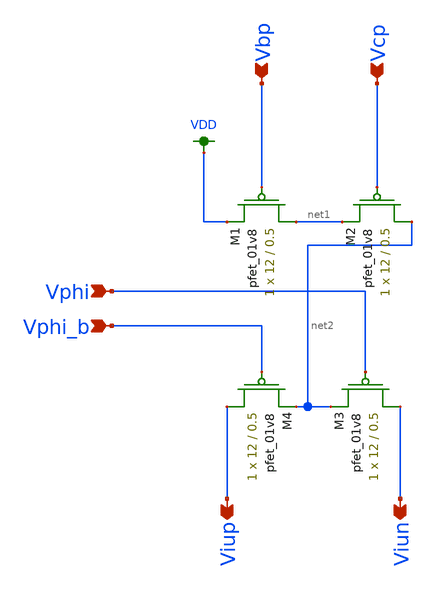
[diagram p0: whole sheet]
** sch_path: simulation/dac/dac_unit_lds.sch
**.subckt dac_unit_lds Vphi Vbp Vcp Viun Viup Vphi_b
*.ipin Vphi
*.ipin Vbp
*.ipin Vcp
*.opin Viun
*.opin Viup
*.ipin Vphi_b
XM1 net1 Vbp VDD VDD sky130_fd_pr__pfet_01v8 L=0.5 W=12 nf=1 ad='int((nf+1)/2) * W/nf * 0.29' as='int((nf+2)/2) * W/nf * 0.29'
+ pd='2*int((nf+1)/2) * (W/nf + 0.29)' ps='2*int((nf+2)/2) * (W/nf + 0.29)' nrd='0.29 / W' nrs='0.29 / W'
+ sa=0 sb=0 sd=0 mult=1 m=1
XM2 net2 Vcp net1 VDD sky130_fd_pr__pfet_01v8 L=0.5 W=12 nf=1 ad='int((nf+1)/2) * W/nf * 0.29' as='int((nf+2)/2) * W/nf * 0.29'
+ pd='2*int((nf+1)/2) * (W/nf + 0.29)' ps='2*int((nf+2)/2) * (W/nf + 0.29)' nrd='0.29 / W' nrs='0.29 / W'
+ sa=0 sb=0 sd=0 mult=1 m=1
XM3 Viun Vphi net2 VDD sky130_fd_pr__pfet_01v8 L=0.5 W=12 nf=1 ad='int((nf+1)/2) * W/nf * 0.29' as='int((nf+2)/2) * W/nf * 0.29'
+ pd='2*int((nf+1)/2) * (W/nf + 0.29)' ps='2*int((nf+2)/2) * (W/nf + 0.29)' nrd='0.29 / W' nrs='0.29 / W'
+ sa=0 sb=0 sd=0 mult=1 m=1
XM4 Viup Vphi_b net2 VDD sky130_fd_pr__pfet_01v8 L=0.5 W=12 nf=1 ad='int((nf+1)/2) * W/nf * 0.29' as='int((nf+2)/2) * W/nf * 0.29'
+ pd='2*int((nf+1)/2) * (W/nf + 0.29)' ps='2*int((nf+2)/2) * (W/nf + 0.29)' nrd='0.29 / W' nrs='0.29 / W'
+ sa=0 sb=0 sd=0 mult=1 m=1
**.ends
.GLOBAL VDD
.end
